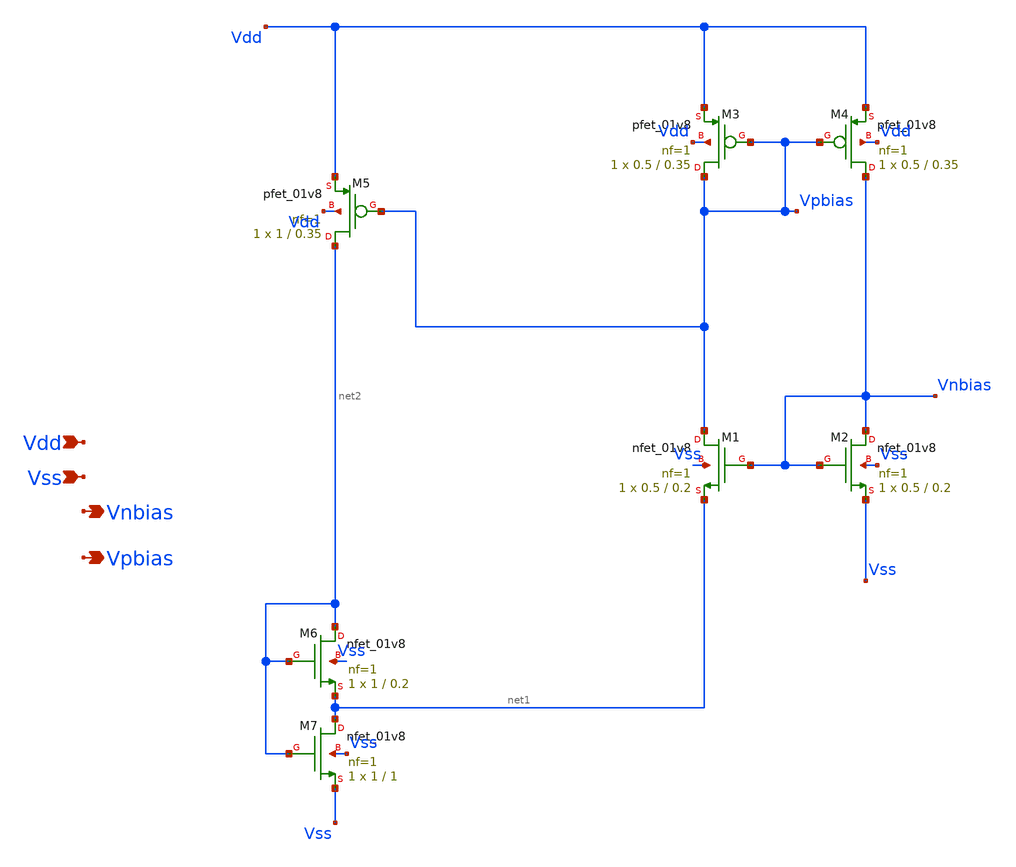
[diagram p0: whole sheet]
** sch_path: tt10-hdl/tt_um_test_commit/xschem/T2/biasGen/A_tt10_10nA/ibias_10nA.sch
**.subckt ibias_10nA Vdd Vss Vnbias Vpbias
*.ipin Vdd
*.ipin Vss
*.opin Vnbias
*.opin Vpbias
XM3 Vpbias Vpbias Vdd Vdd sky130_fd_pr__pfet_01v8 L=0.35 W=0.5 nf=1 ad='int((nf+1)/2) * W/nf * 0.29'
+ as='int((nf+2)/2) * W/nf * 0.29' pd='2*int((nf+1)/2) * (W/nf + 0.29)' ps='2*int((nf+2)/2) * (W/nf + 0.29)'
+ nrd='0.29 / W' nrs='0.29 / W' sa=0 sb=0 sd=0 mult=1 m=1
XM4 Vnbias Vpbias Vdd Vdd sky130_fd_pr__pfet_01v8 L=0.35 W=0.5 nf=1 ad='int((nf+1)/2) * W/nf * 0.29'
+ as='int((nf+2)/2) * W/nf * 0.29' pd='2*int((nf+1)/2) * (W/nf + 0.29)' ps='2*int((nf+2)/2) * (W/nf + 0.29)'
+ nrd='0.29 / W' nrs='0.29 / W' sa=0 sb=0 sd=0 mult=1 m=1
XM5 net2 Vpbias Vdd Vdd sky130_fd_pr__pfet_01v8 L=0.35 W=1 nf=1 ad='int((nf+1)/2) * W/nf * 0.29' as='int((nf+2)/2) * W/nf * 0.29'
+ pd='2*int((nf+1)/2) * (W/nf + 0.29)' ps='2*int((nf+2)/2) * (W/nf + 0.29)' nrd='0.29 / W' nrs='0.29 / W'
+ sa=0 sb=0 sd=0 mult=1 m=1
XM1 Vpbias Vnbias net1 Vss sky130_fd_pr__nfet_01v8 L=0.2 W=0.5 nf=1 ad='int((1 + 1)/2) * 0.5 / 1 * 0.29'
+ as='int((1 + 2)/2) * 0.5 / 1 * 0.29' pd='2*int((1 + 1)/2) * (0.5 / 1 + 0.29)' ps='2*int((1 + 2)/2) * (0.5 / 1 + 0.29)'
+ nrd='0.29 / 0.5 ' nrs='0.29 / 0.5 ' sa=0 sb=0 sd=0 mult=1 m=1
XM2 Vnbias Vnbias Vss Vss sky130_fd_pr__nfet_01v8 L=0.2 W=0.5 nf=1 ad='int((1 + 1)/2) * 0.5 / 1 * 0.29'
+ as='int((1 + 2)/2) * 0.5 / 1 * 0.29' pd='2*int((1 + 1)/2) * (0.5 / 1 + 0.29)' ps='2*int((1 + 2)/2) * (0.5 / 1 + 0.29)'
+ nrd='0.29 / 0.5 ' nrs='0.29 / 0.5 ' sa=0 sb=0 sd=0 mult=1 m=1
XM6 net2 net2 net1 Vss sky130_fd_pr__nfet_01v8 L=0.2 W=1 nf=1 ad='int((1 + 1)/2) * 1 / 1 * 0.29' as='int((1 + 2)/2) * 1 / 1 * 0.29'
+ pd='2*int((1 + 1)/2) * (1 / 1 + 0.29)' ps='2*int((1 + 2)/2) * (1 / 1 + 0.29)' nrd='0.29 / 1 ' nrs='0.29 / 1 '
+ sa=0 sb=0 sd=0 mult=1 m=1
XM7 net1 net2 Vss Vss sky130_fd_pr__nfet_01v8 L=1 W=1 nf=1 ad='int((1 + 1)/2) * 1 / 1 * 0.29' as='int((1 + 2)/2) * 1 / 1 * 0.29'
+ pd='2*int((1 + 1)/2) * (1 / 1 + 0.29)' ps='2*int((1 + 2)/2) * (1 / 1 + 0.29)' nrd='0.29 / 1 ' nrs='0.29 / 1 '
+ sa=0 sb=0 sd=0 mult=1 m=1
**.ends
.end
